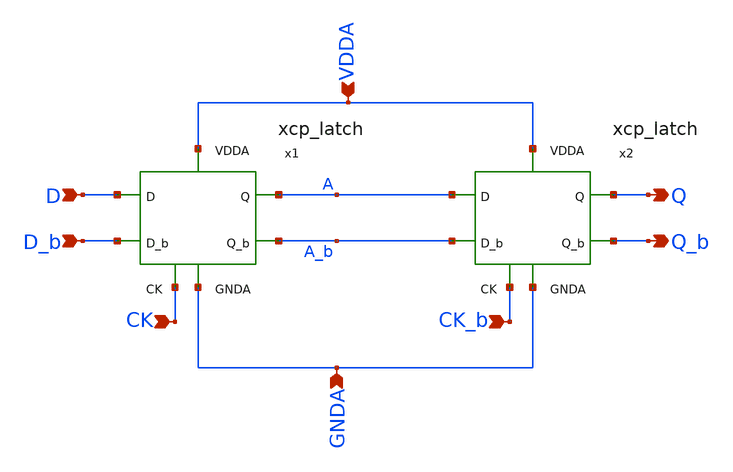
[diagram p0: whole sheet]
** sch_path: projects/pll/divider/xschem_ngspice/xcp_FF.sch
**.subckt xcp_FF VDDA Q CK GNDA Q_b CK_b D D_b
*.ipin VDDA
*.opin Q
*.ipin CK
*.ipin GNDA
*.opin Q_b
*.ipin CK_b
*.ipin D
*.ipin D_b
x2 VDDA Q_b Q A_b A CK_b GNDA xcp_latch
x1 VDDA A_b A D_b D CK GNDA xcp_latch
**.ends

* expanding   symbol:  /foss/designs/my_design/projects/pll/divider/xschem_ngspice/xcp_latch.sym #
*+ of pins=7
** sym_path: projects/pll/divider/xschem_ngspice/xcp_latch.sym
** sch_path: projects/pll/divider/xschem_ngspice/xcp_latch.sch
.subckt xcp_latch VDDA Q_b Q D_b D CK GNDA
*.ipin D
*.opin Q
*.ipin D_b
*.ipin CK
*.opin Q_b
*.ipin VDDA
*.ipin GNDA
XM5 net1 CK GNDA GNDA sky130_fd_pr__nfet_01v8 L=0.15 W=2 nf=2 ad='int((nf+1)/2) * W/nf * 0.29' as='int((nf+2)/2) * W/nf * 0.29'
+ pd='2*int((nf+1)/2) * (W/nf + 0.29)' ps='2*int((nf+2)/2) * (W/nf + 0.29)' nrd='0.29 / W' nrs='0.29 / W'
+ sa=0 sb=0 sd=0 mult=1 m=1
XM1 net3 D V_common GNDA sky130_fd_pr__nfet_01v8 L=0.15 W=1 nf=1 ad='int((nf+1)/2) * W/nf * 0.29' as='int((nf+2)/2) * W/nf * 0.29'
+ pd='2*int((nf+1)/2) * (W/nf + 0.29)' ps='2*int((nf+2)/2) * (W/nf + 0.29)' nrd='0.29 / W' nrs='0.29 / W'
+ sa=0 sb=0 sd=0 mult=1 m=1
XM2 net2 D_b V_common GNDA sky130_fd_pr__nfet_01v8 L=0.15 W=1 nf=1 ad='int((nf+1)/2) * W/nf * 0.29' as='int((nf+2)/2) * W/nf * 0.29'
+ pd='2*int((nf+1)/2) * (W/nf + 0.29)' ps='2*int((nf+2)/2) * (W/nf + 0.29)' nrd='0.29 / W' nrs='0.29 / W'
+ sa=0 sb=0 sd=0 mult=1 m=1
Vmeas V_common net1 0
.save i(vmeas)
Vmeas1 Q_b net3 0
.save i(vmeas1)
Vmeas2 Q net2 0
.save i(vmeas2)
XM3 Q_b Q VDDA VDDA sky130_fd_pr__pfet_01v8 L=0.15 W=1 nf=1 ad='int((nf+1)/2) * W/nf * 0.29' as='int((nf+2)/2) * W/nf * 0.29'
+ pd='2*int((nf+1)/2) * (W/nf + 0.29)' ps='2*int((nf+2)/2) * (W/nf + 0.29)' nrd='0.29 / W' nrs='0.29 / W'
+ sa=0 sb=0 sd=0 mult=1 m=1
XM4 Q Q_b VDDA VDDA sky130_fd_pr__pfet_01v8 L=0.15 W=1 nf=1 ad='int((nf+1)/2) * W/nf * 0.29' as='int((nf+2)/2) * W/nf * 0.29'
+ pd='2*int((nf+1)/2) * (W/nf + 0.29)' ps='2*int((nf+2)/2) * (W/nf + 0.29)' nrd='0.29 / W' nrs='0.29 / W'
+ sa=0 sb=0 sd=0 mult=1 m=1
.ends

.end
